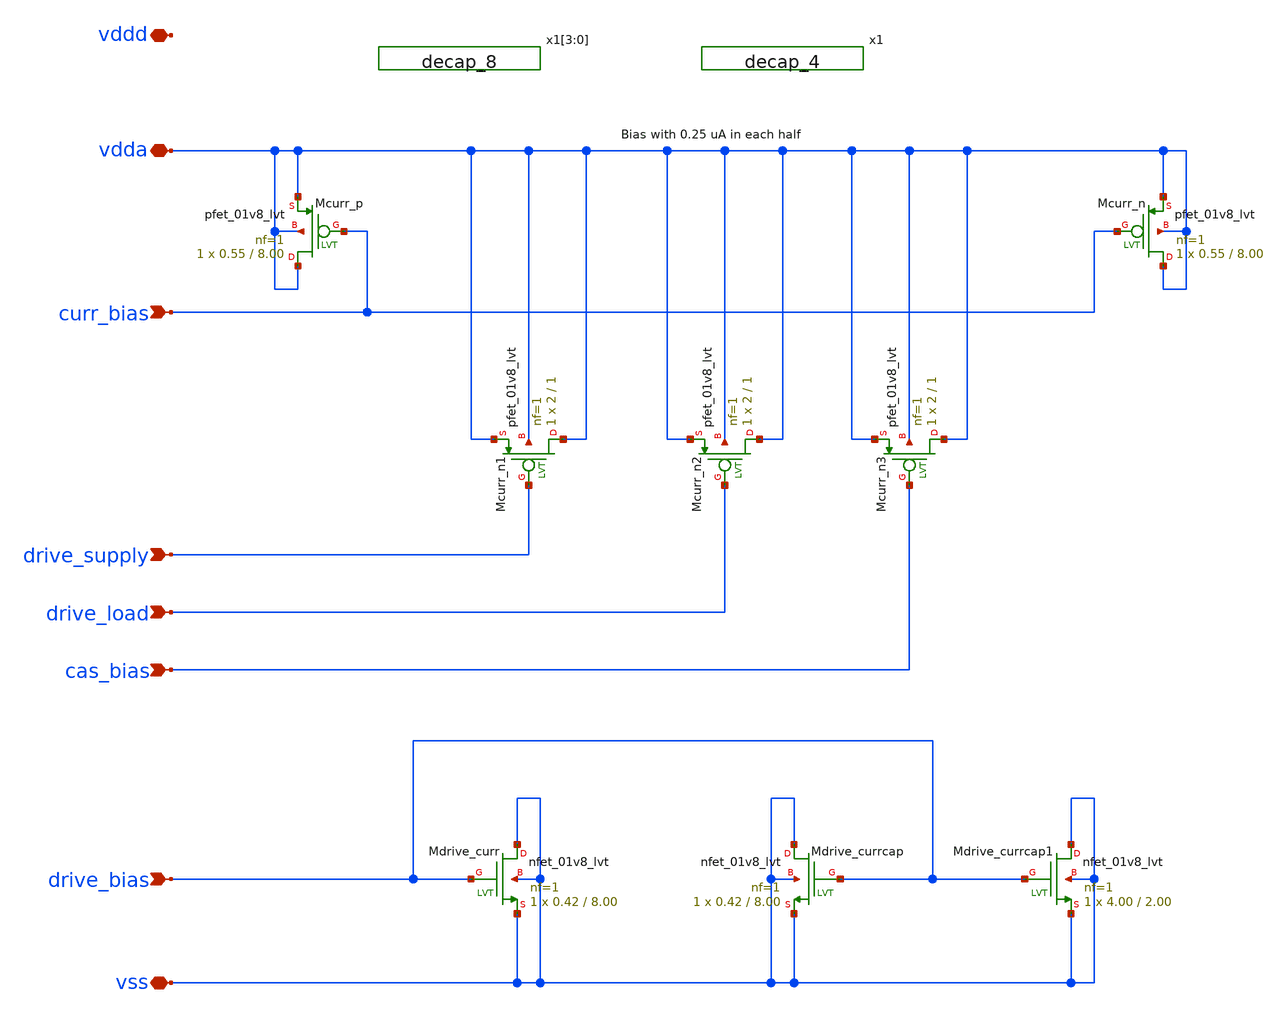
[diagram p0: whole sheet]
** sch_path: design/dac_unit_cell_dummy/dac_unit_cell_dummy.sch
**.subckt dac_unit_cell_dummy vdda vss curr_bias drive_supply cas_bias drive_bias drive_load vddd
*.iopin vdda
*.iopin vss
*.ipin curr_bias
*.ipin drive_supply
*.ipin cas_bias
*.ipin drive_bias
*.ipin drive_load
*.iopin vddd
XMcurr_p vdda curr_bias vdda vdda sky130_fd_pr__pfet_01v8_lvt L=8.00 W=0.55 nf=1 ad='int((nf+1)/2) * W/nf * 0.29'
+ as='int((nf+2)/2) * W/nf * 0.29' pd='2*int((nf+1)/2) * (W/nf + 0.29)' ps='2*int((nf+2)/2) * (W/nf + 0.29)'
+ nrd='0.29 / W' nrs='0.29 / W' sa=0 sb=0 sd=0 mult=1 m=1
XMcurr_n vdda curr_bias vdda vdda sky130_fd_pr__pfet_01v8_lvt L=8.00 W=0.55 nf=1 ad='int((nf+1)/2) * W/nf * 0.29'
+ as='int((nf+2)/2) * W/nf * 0.29' pd='2*int((nf+1)/2) * (W/nf + 0.29)' ps='2*int((nf+2)/2) * (W/nf + 0.29)'
+ nrd='0.29 / W' nrs='0.29 / W' sa=0 sb=0 sd=0 mult=1 m=1
XMdrive_curr vss drive_bias vss vss sky130_fd_pr__nfet_01v8_lvt L=8.00 W=0.42 nf=1 ad='int((nf+1)/2) * W/nf * 0.29'
+ as='int((nf+2)/2) * W/nf * 0.29' pd='2*int((nf+1)/2) * (W/nf + 0.29)' ps='2*int((nf+2)/2) * (W/nf + 0.29)'
+ nrd='0.29 / W' nrs='0.29 / W' sa=0 sb=0 sd=0 mult=1 m=1
XMdrive_currcap vss drive_bias vss vss sky130_fd_pr__nfet_01v8_lvt L=8.00 W=0.42 nf=1 ad='int((nf+1)/2) * W/nf * 0.29'
+ as='int((nf+2)/2) * W/nf * 0.29' pd='2*int((nf+1)/2) * (W/nf + 0.29)' ps='2*int((nf+2)/2) * (W/nf + 0.29)'
+ nrd='0.29 / W' nrs='0.29 / W' sa=0 sb=0 sd=0 mult=1 m=1
XMdrive_currcap1 vss drive_bias vss vss sky130_fd_pr__nfet_01v8_lvt L=2.00 W=4.00 nf=1 ad='int((nf+1)/2) * W/nf * 0.29'
+ as='int((nf+2)/2) * W/nf * 0.29' pd='2*int((nf+1)/2) * (W/nf + 0.29)' ps='2*int((nf+2)/2) * (W/nf + 0.29)'
+ nrd='0.29 / W' nrs='0.29 / W' sa=0 sb=0 sd=0 mult=1 m=1
XMcurr_n1 vdda drive_supply vdda vdda sky130_fd_pr__pfet_01v8_lvt L=1 W=2 nf=1 ad='int((nf+1)/2) * W/nf * 0.29'
+ as='int((nf+2)/2) * W/nf * 0.29' pd='2*int((nf+1)/2) * (W/nf + 0.29)' ps='2*int((nf+2)/2) * (W/nf + 0.29)'
+ nrd='0.29 / W' nrs='0.29 / W' sa=0 sb=0 sd=0 mult=1 m=1
XMcurr_n2 vdda drive_load vdda vdda sky130_fd_pr__pfet_01v8_lvt L=1 W=2 nf=1 ad='int((nf+1)/2) * W/nf * 0.29'
+ as='int((nf+2)/2) * W/nf * 0.29' pd='2*int((nf+1)/2) * (W/nf + 0.29)' ps='2*int((nf+2)/2) * (W/nf + 0.29)'
+ nrd='0.29 / W' nrs='0.29 / W' sa=0 sb=0 sd=0 mult=1 m=1
XMcurr_n3 vdda cas_bias vdda vdda sky130_fd_pr__pfet_01v8_lvt L=1 W=2 nf=1 ad='int((nf+1)/2) * W/nf * 0.29'
+ as='int((nf+2)/2) * W/nf * 0.29' pd='2*int((nf+1)/2) * (W/nf + 0.29)' ps='2*int((nf+2)/2) * (W/nf + 0.29)'
+ nrd='0.29 / W' nrs='0.29 / W' sa=0 sb=0 sd=0 mult=1 m=1
x1[3] vss vss vddd vddd sky130_fd_sc_hs__decap_8
x1[2] vss vss vddd vddd sky130_fd_sc_hs__decap_8
x1[1] vss vss vddd vddd sky130_fd_sc_hs__decap_8
x1[0] vss vss vddd vddd sky130_fd_sc_hs__decap_8
x1 vss vss vddd vddd sky130_fd_sc_hs__decap_4
**.ends
.end
